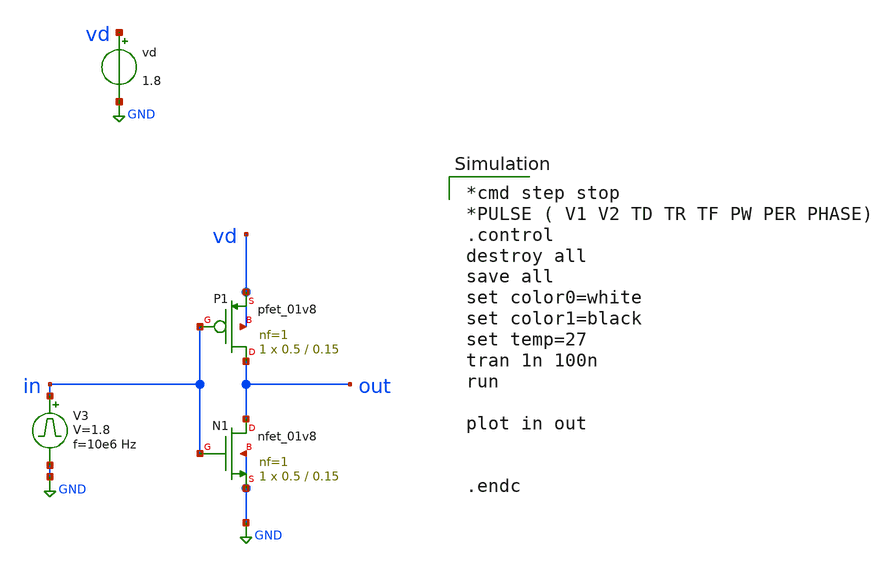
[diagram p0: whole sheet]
** sch_path: mag/sigma-delta_modulator/xschem/inv_tb-tran.sch
**.subckt inv_tb-tran
V3 in GND pulse 0 1.8 '0.495/ 10e6 ' '0.01/10e6 ' '0.01/10e6 ' '0.49/10e6 ' '1/10e6 '
vd vd GND 1.8
XN1 out in GND GND sky130_fd_pr__nfet_01v8 L=0.15 W=0.5 nf=1 ad='int((nf+1)/2) * W/nf * 0.29' as='int((nf+2)/2) * W/nf * 0.29'
+ pd='2*int((nf+1)/2) * (W/nf + 0.29)' ps='2*int((nf+2)/2) * (W/nf + 0.29)' nrd='0.29 / W' nrs='0.29 / W'
+ sa=0 sb=0 sd=0 mult=1 m=1
XP1 out in vd vd sky130_fd_pr__pfet_01v8 L=0.15 W=0.5 nf=1 ad='int((nf+1)/2) * W/nf * 0.29' as='int((nf+2)/2) * W/nf * 0.29'
+ pd='2*int((nf+1)/2) * (W/nf + 0.29)' ps='2*int((nf+2)/2) * (W/nf + 0.29)' nrd='0.29 / W' nrs='0.29 / W'
+ sa=0 sb=0 sd=0 mult=1 m=1
**** begin user architecture code

*cmd step stop
*PULSE ( V1 V2 TD TR TF PW PER PHASE)
.control
destroy all
save all
set color0=white
set color1=black
set temp=27
tran 1n 100n
run

plot in out


.endc

 .lib $::SKYWATER_MODELS/sky130.lib.spice tt
.include $::SKYWATER_STDCELLS/sky130_fd_sc_hd.spice

**** end user architecture code
**.ends
.GLOBAL GND
.end
